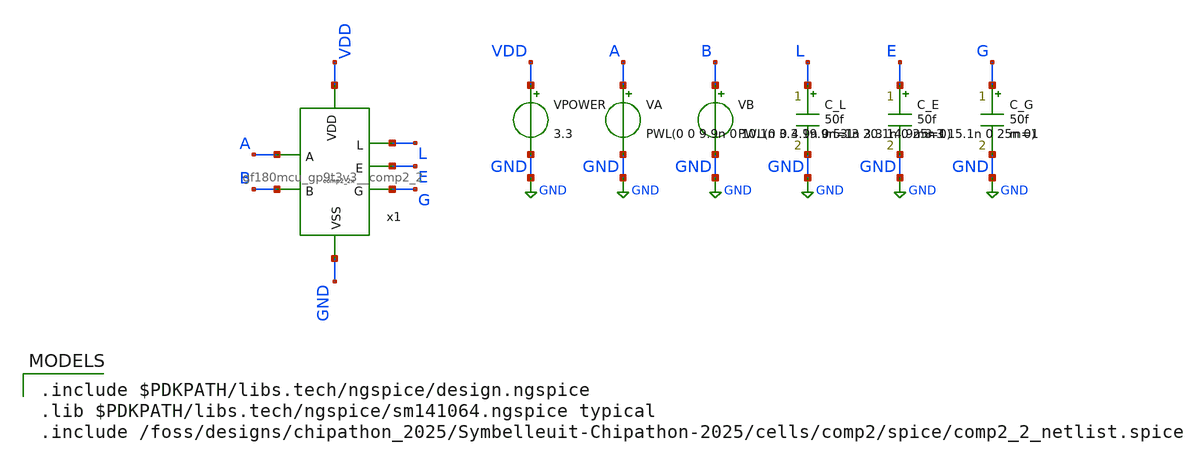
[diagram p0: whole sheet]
** sch_path: cells/comp2/cace/templates/comp2_2_tb_func.sch
**.subckt comp2_2_tb_func
x1 VDD L A E G B GND gf180mcu_gp9t3v3__comp2_2
VPOWER VDD GND 3.3
VA A GND PWL(0 0 9.9n 0 10.1n 3.3 19.9n 3.3 20.1n 0 25n 0)
VB B GND PWL(0 0 4.9n 0 5.1n 3.3 14.9n 3.3 15.1n 0 25n 0)
C_L L GND 50f m=1
C_E E GND 50f m=1
C_G G GND 50f m=1
**** begin user architecture code

.include $PDKPATH/libs.tech/ngspice/design.ngspice
.lib $PDKPATH/libs.tech/ngspice/sm141064.ngspice typical
.include /foss/designs/chipathon_2025/Symbelleuit-Chipathon-2025/cells/comp2/spice/comp2_2_netlist.spice


* CACE Functional Truth-Table Error Simulation
.tran 100p 25n
.control
  run
  * State 00: A=0, B=0 -> L=0, E=3.3, G=0
  meas tran v_L_00 FIND v(L) AT=2.5n
  meas tran v_E_00 FIND v(E) AT=2.5n
  meas tran v_G_00 FIND v(G) AT=2.5n

  * State 01: A=0, B=1 -> L=3.3, E=0, G=0
  meas tran v_L_01 FIND v(L) AT=7.5n
  meas tran v_E_01 FIND v(E) AT=7.5n
  meas tran v_G_01 FIND v(G) AT=7.5n

  * State 11: A=1, B=1 -> L=0, E=3.3, G=0
  meas tran v_L_11 FIND v(L) AT=12.5n
  meas tran v_E_11 FIND v(E) AT=12.5n
  meas tran v_G_11 FIND v(G) AT=12.5n

  * State 10: A=1, B=0 -> L=0, E=0, G=3.3
  meas tran v_L_10 FIND v(L) AT=17.5n
  meas tran v_E_10 FIND v(E) AT=17.5n
  meas tran v_G_10 FIND v(G) AT=17.5n

  let err_00 = v_L_00 + abs(v_E_00 - 3.3) + v_G_00
  let err_01 = abs(v_L_01 - 3.3) + v_E_01 + v_G_01
  let err_11 = v_L_11 + abs(v_E_11 - 3.3) + v_G_11
  let err_10 = v_L_10 + v_E_10 + abs(v_G_10 - 3.3)
  let func_total_err = err_00 + err_01 + err_11 + err_10
  print func_total_err
  echo $&func_total_err > comp2_2_tb_func_0.data
.endc
.GLOBAL GND


**** end user architecture code
**.ends

* expanding   symbol:  gf180mcu_gp9t3v3__comp2_2.sym # of pins=7
** sym_path: integration/cells/gf180mcu_gp9t3v3__comp2_2.sym
** sch_path: integration/cells/gf180mcu_gp9t3v3__comp2_2.sch
.subckt gf180mcu_gp9t3v3__comp2_2 VDD L A E G B VSS
*.opin L
*.opin G
*.opin E
*.ipin A
*.ipin B
*.ipin VDD
*.ipin VSS
XM17 net1 NOT_A VDD VDD pfet_03v3 L=0.3u W=1.7u nf=1 ad='int((nf+1)/2) * W/nf * 0.18u' as='int((nf+2)/2) * W/nf * 0.18u'
+ pd='2*int((nf+1)/2) * (W/nf + 0.18u)' ps='2*int((nf+2)/2) * (W/nf + 0.18u)' nrd='0.18u / W' nrs='0.18u / W'
+ sa=0 sb=0 sd=0 m=1
XM18 E NOT_B net1 VDD pfet_03v3 L=0.3u W=1.7u nf=1 ad='int((nf+1)/2) * W/nf * 0.18u' as='int((nf+2)/2) * W/nf * 0.18u'
+ pd='2*int((nf+1)/2) * (W/nf + 0.18u)' ps='2*int((nf+2)/2) * (W/nf + 0.18u)' nrd='0.18u / W' nrs='0.18u / W'
+ sa=0 sb=0 sd=0 m=1
XM19 net1 B VDD VDD pfet_03v3 L=0.3u W=3.4u nf=2 ad='int((nf+1)/2) * W/nf * 0.18u' as='int((nf+2)/2) * W/nf * 0.18u'
+ pd='2*int((nf+1)/2) * (W/nf + 0.18u)' ps='2*int((nf+2)/2) * (W/nf + 0.18u)' nrd='0.18u / W' nrs='0.18u / W'
+ sa=0 sb=0 sd=0 m=1
XM20 E A net1 VDD pfet_03v3 L=0.3u W=3.4u nf=2 ad='int((nf+1)/2) * W/nf * 0.18u' as='int((nf+2)/2) * W/nf * 0.18u'
+ pd='2*int((nf+1)/2) * (W/nf + 0.18u)' ps='2*int((nf+2)/2) * (W/nf + 0.18u)' nrd='0.18u / W' nrs='0.18u / W'
+ sa=0 sb=0 sd=0 m=1
XM21 E NOT_A net2 VSS nfet_03v3 L=0.3u W=0.85u nf=1 ad='int((nf+1)/2) * W/nf * 0.18u' as='int((nf+2)/2) * W/nf * 0.18u'
+ pd='2*int((nf+1)/2) * (W/nf + 0.18u)' ps='2*int((nf+2)/2) * (W/nf + 0.18u)' nrd='0.18u / W' nrs='0.18u / W'
+ sa=0 sb=0 sd=0 m=1
XM22 net2 B VSS VSS nfet_03v3 L=0.3u W=0.85u nf=1 ad='int((nf+1)/2) * W/nf * 0.18u' as='int((nf+2)/2) * W/nf * 0.18u'
+ pd='2*int((nf+1)/2) * (W/nf + 0.18u)' ps='2*int((nf+2)/2) * (W/nf + 0.18u)' nrd='0.18u / W' nrs='0.18u / W'
+ sa=0 sb=0 sd=0 m=1
XM23 E A net3 VSS nfet_03v3 L=0.3u W=1.7u nf=2 ad='int((nf+1)/2) * W/nf * 0.18u' as='int((nf+2)/2) * W/nf * 0.18u'
+ pd='2*int((nf+1)/2) * (W/nf + 0.18u)' ps='2*int((nf+2)/2) * (W/nf + 0.18u)' nrd='0.18u / W' nrs='0.18u / W'
+ sa=0 sb=0 sd=0 m=1
XM24 net3 NOT_B VSS VSS nfet_03v3 L=0.3u W=1.7u nf=2 ad='int((nf+1)/2) * W/nf * 0.18u' as='int((nf+2)/2) * W/nf * 0.18u'
+ pd='2*int((nf+1)/2) * (W/nf + 0.18u)' ps='2*int((nf+2)/2) * (W/nf + 0.18u)' nrd='0.18u / W' nrs='0.18u / W'
+ sa=0 sb=0 sd=0 m=1
XM1 NOT_B B VSS VSS nfet_03v3 L=0.3u W=0.85u nf=1 ad='int((nf+1)/2) * W/nf * 0.18u' as='int((nf+2)/2) * W/nf * 0.18u'
+ pd='2*int((nf+1)/2) * (W/nf + 0.18u)' ps='2*int((nf+2)/2) * (W/nf + 0.18u)' nrd='0.18u / W' nrs='0.18u / W'
+ sa=0 sb=0 sd=0 m=1
XM2 NOT_B B VDD VDD pfet_03v3 L=0.3u W=1.7u nf=1 ad='int((nf+1)/2) * W/nf * 0.18u' as='int((nf+2)/2) * W/nf * 0.18u'
+ pd='2*int((nf+1)/2) * (W/nf + 0.18u)' ps='2*int((nf+2)/2) * (W/nf + 0.18u)' nrd='0.18u / W' nrs='0.18u / W'
+ sa=0 sb=0 sd=0 m=1
XM3 NOT_A A VSS VSS nfet_03v3 L=0.3u W=0.85u nf=1 ad='int((nf+1)/2) * W/nf * 0.18u' as='int((nf+2)/2) * W/nf * 0.18u'
+ pd='2*int((nf+1)/2) * (W/nf + 0.18u)' ps='2*int((nf+2)/2) * (W/nf + 0.18u)' nrd='0.18u / W' nrs='0.18u / W'
+ sa=0 sb=0 sd=0 m=1
XM4 NOT_A A VDD VDD pfet_03v3 L=0.3u W=1.7u nf=1 ad='int((nf+1)/2) * W/nf * 0.18u' as='int((nf+2)/2) * W/nf * 0.18u'
+ pd='2*int((nf+1)/2) * (W/nf + 0.18u)' ps='2*int((nf+2)/2) * (W/nf + 0.18u)' nrd='0.18u / W' nrs='0.18u / W'
+ sa=0 sb=0 sd=0 m=1
XM5 net5 NOT_A net4 VSS nfet_03v3 L=0.3u W=0.85u nf=1 ad='int((nf+1)/2) * W/nf * 0.18u' as='int((nf+2)/2) * W/nf * 0.18u'
+ pd='2*int((nf+1)/2) * (W/nf + 0.18u)' ps='2*int((nf+2)/2) * (W/nf + 0.18u)' nrd='0.18u / W' nrs='0.18u / W'
+ sa=0 sb=0 sd=0 m=1
XM6 net4 B VSS VSS nfet_03v3 L=0.3u W=0.85u nf=1 ad='int((nf+1)/2) * W/nf * 0.18u' as='int((nf+2)/2) * W/nf * 0.18u'
+ pd='2*int((nf+1)/2) * (W/nf + 0.18u)' ps='2*int((nf+2)/2) * (W/nf + 0.18u)' nrd='0.18u / W' nrs='0.18u / W'
+ sa=0 sb=0 sd=0 m=1
XM7 net5 B VDD VDD pfet_03v3 L=0.3u W=1.7u nf=1 ad='int((nf+1)/2) * W/nf * 0.18u' as='int((nf+2)/2) * W/nf * 0.18u'
+ pd='2*int((nf+1)/2) * (W/nf + 0.18u)' ps='2*int((nf+2)/2) * (W/nf + 0.18u)' nrd='0.18u / W' nrs='0.18u / W'
+ sa=0 sb=0 sd=0 m=1
XM8 net5 NOT_A VDD VDD pfet_03v3 L=0.3u W=1.7u nf=1 ad='int((nf+1)/2) * W/nf * 0.18u' as='int((nf+2)/2) * W/nf * 0.18u'
+ pd='2*int((nf+1)/2) * (W/nf + 0.18u)' ps='2*int((nf+2)/2) * (W/nf + 0.18u)' nrd='0.18u / W' nrs='0.18u / W'
+ sa=0 sb=0 sd=0 m=1
XM9 L net5 VSS VSS nfet_03v3 L=0.3u W=1.7u nf=2 ad='int((nf+1)/2) * W/nf * 0.18u' as='int((nf+2)/2) * W/nf * 0.18u'
+ pd='2*int((nf+1)/2) * (W/nf + 0.18u)' ps='2*int((nf+2)/2) * (W/nf + 0.18u)' nrd='0.18u / W' nrs='0.18u / W'
+ sa=0 sb=0 sd=0 m=1
XM10 L net5 VDD VDD pfet_03v3 L=0.3u W=3.4u nf=2 ad='int((nf+1)/2) * W/nf * 0.18u' as='int((nf+2)/2) * W/nf * 0.18u'
+ pd='2*int((nf+1)/2) * (W/nf + 0.18u)' ps='2*int((nf+2)/2) * (W/nf + 0.18u)' nrd='0.18u / W' nrs='0.18u / W'
+ sa=0 sb=0 sd=0 m=1
XM11 net7 NOT_B net6 VSS nfet_03v3 L=0.3u W=0.85u nf=1 ad='int((nf+1)/2) * W/nf * 0.18u' as='int((nf+2)/2) * W/nf * 0.18u'
+ pd='2*int((nf+1)/2) * (W/nf + 0.18u)' ps='2*int((nf+2)/2) * (W/nf + 0.18u)' nrd='0.18u / W' nrs='0.18u / W'
+ sa=0 sb=0 sd=0 m=1
XM12 net6 A VSS VSS nfet_03v3 L=0.3u W=0.85u nf=1 ad='int((nf+1)/2) * W/nf * 0.18u' as='int((nf+2)/2) * W/nf * 0.18u'
+ pd='2*int((nf+1)/2) * (W/nf + 0.18u)' ps='2*int((nf+2)/2) * (W/nf + 0.18u)' nrd='0.18u / W' nrs='0.18u / W'
+ sa=0 sb=0 sd=0 m=1
XM13 net7 NOT_B VDD VDD pfet_03v3 L=0.3u W=1.7u nf=1 ad='int((nf+1)/2) * W/nf * 0.18u' as='int((nf+2)/2) * W/nf * 0.18u'
+ pd='2*int((nf+1)/2) * (W/nf + 0.18u)' ps='2*int((nf+2)/2) * (W/nf + 0.18u)' nrd='0.18u / W' nrs='0.18u / W'
+ sa=0 sb=0 sd=0 m=1
XM14 net7 A VDD VDD pfet_03v3 L=0.3u W=1.7u nf=1 ad='int((nf+1)/2) * W/nf * 0.18u' as='int((nf+2)/2) * W/nf * 0.18u'
+ pd='2*int((nf+1)/2) * (W/nf + 0.18u)' ps='2*int((nf+2)/2) * (W/nf + 0.18u)' nrd='0.18u / W' nrs='0.18u / W'
+ sa=0 sb=0 sd=0 m=1
XM15 G net7 VSS VSS nfet_03v3 L=0.3u W=1.7u nf=2 ad='int((nf+1)/2) * W/nf * 0.18u' as='int((nf+2)/2) * W/nf * 0.18u'
+ pd='2*int((nf+1)/2) * (W/nf + 0.18u)' ps='2*int((nf+2)/2) * (W/nf + 0.18u)' nrd='0.18u / W' nrs='0.18u / W'
+ sa=0 sb=0 sd=0 m=1
XM16 G net7 VDD VDD pfet_03v3 L=0.3u W=3.4u nf=2 ad='int((nf+1)/2) * W/nf * 0.18u' as='int((nf+2)/2) * W/nf * 0.18u'
+ pd='2*int((nf+1)/2) * (W/nf + 0.18u)' ps='2*int((nf+2)/2) * (W/nf + 0.18u)' nrd='0.18u / W' nrs='0.18u / W'
+ sa=0 sb=0 sd=0 m=1
.ends

.GLOBAL GND
.end
